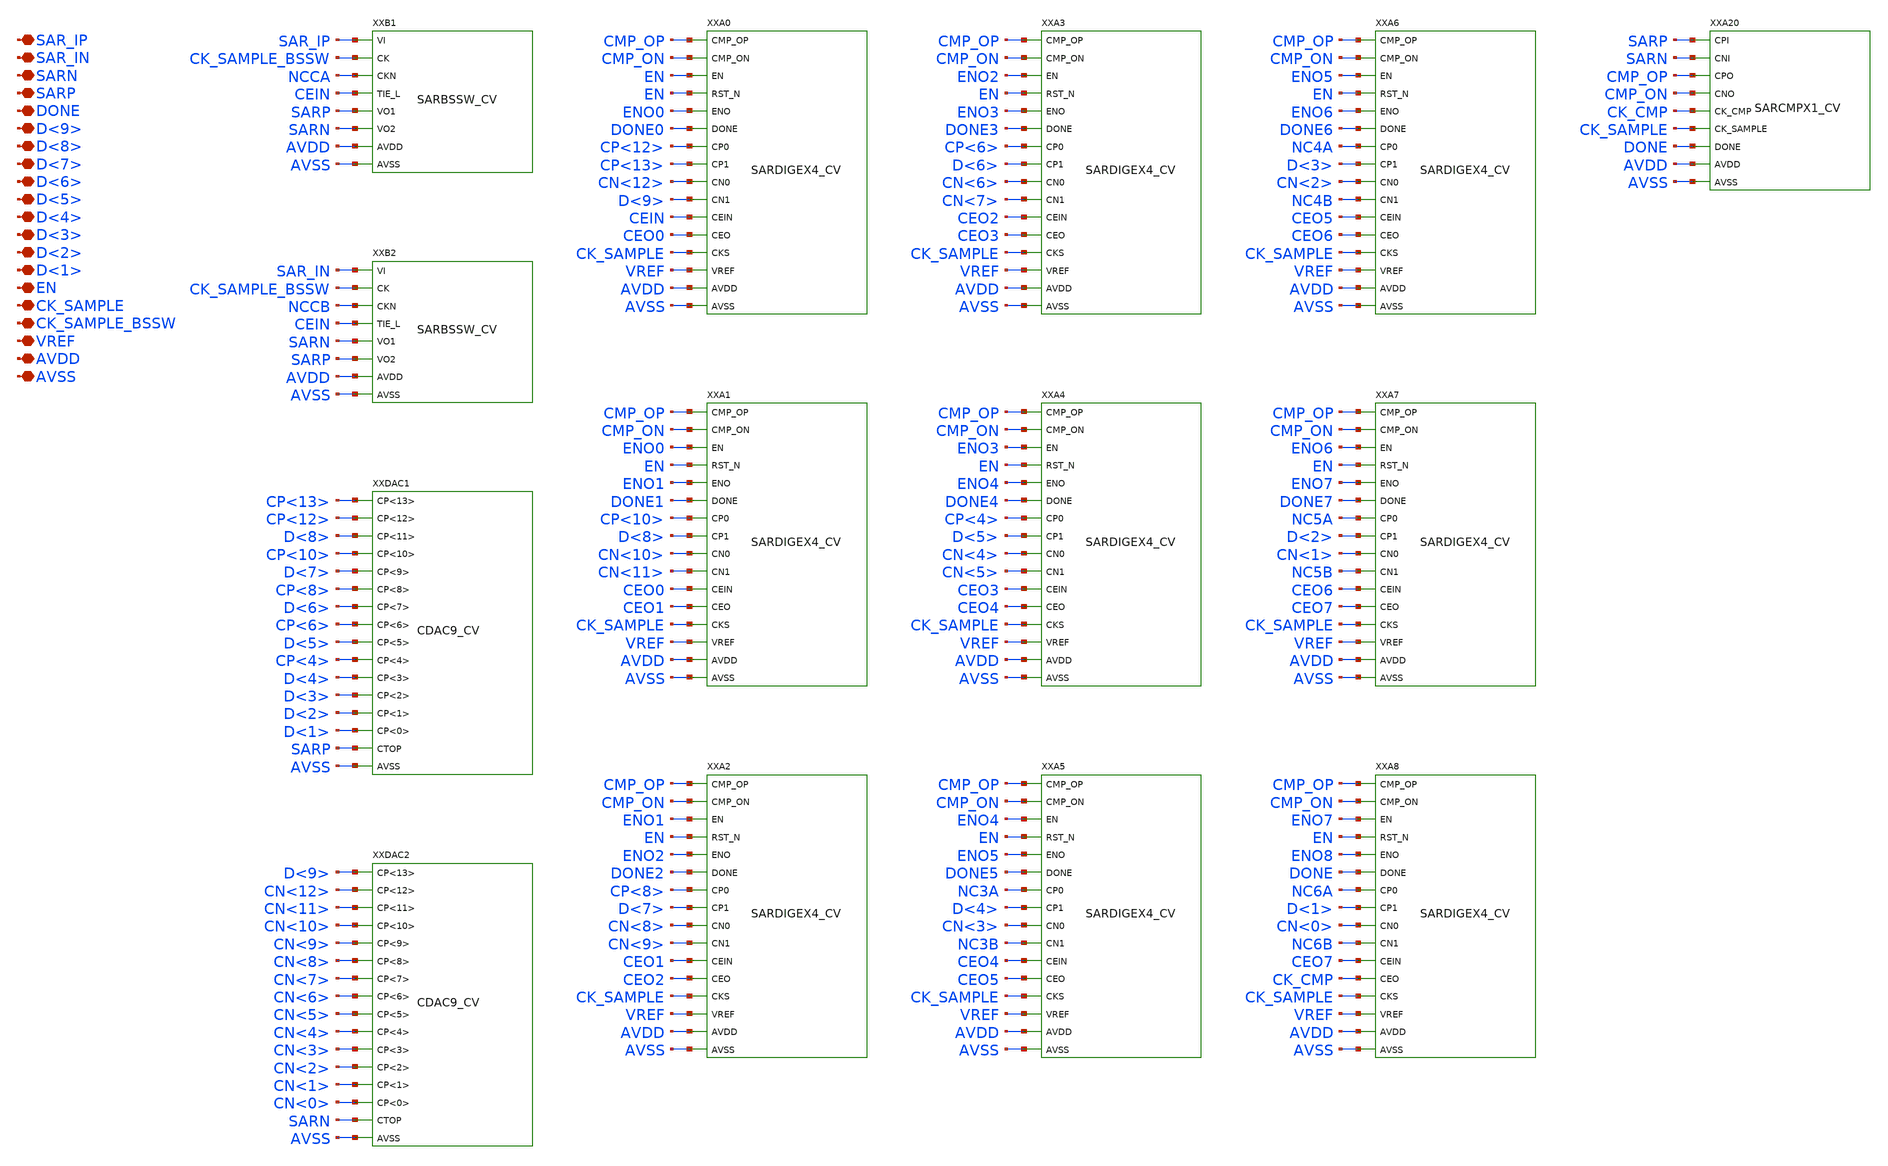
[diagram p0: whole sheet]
** sch_path: tests/transpile/SAR9B/ALGIC001_SAR9B_CV_NOROUTE.sch
**.subckt ALGIC001_SAR9B_CV_NOROUTE SAR_IP SAR_IN SARN SARP DONE D<9> D<8> D<7> D<6> D<5> D<4> D<3>
*+ D<2> D<1> EN CK_SAMPLE CK_SAMPLE_BSSW VREF AVDD AVSS
*.iopin SAR_IP
*.iopin SAR_IN
*.iopin SARN
*.iopin SARP
*.iopin DONE
*.iopin D<9>
*.iopin D<8>
*.iopin D<7>
*.iopin D<6>
*.iopin D<5>
*.iopin D<4>
*.iopin D<3>
*.iopin D<2>
*.iopin D<1>
*.iopin EN
*.iopin CK_SAMPLE
*.iopin CK_SAMPLE_BSSW
*.iopin VREF
*.iopin AVDD
*.iopin AVSS
XXB1 SAR_IP CK_SAMPLE_BSSW NCCA CEIN SARP SARN AVDD AVSS SARBSSW_CV
XXB2 SAR_IN CK_SAMPLE_BSSW NCCB CEIN SARN SARP AVDD AVSS SARBSSW_CV
XXDAC1 CP<13> CP<12> D<8> CP<10> D<7> CP<8> D<6> CP<6> D<5> CP<4> D<4> D<3> D<2> D<1> SARP AVSS
+ CDAC9_CV
XXDAC2 D<9> CN<12> CN<11> CN<10> CN<9> CN<8> CN<7> CN<6> CN<5> CN<4> CN<3> CN<2> CN<1> CN<0> SARN
+ AVSS CDAC9_CV
XXA0 CMP_OP CMP_ON EN EN ENO0 DONE0 CP<12> CP<13> CN<12> D<9> CEIN CEO0 CK_SAMPLE VREF AVDD AVSS
+ SARDIGEX4_CV
XXA1 CMP_OP CMP_ON ENO0 EN ENO1 DONE1 CP<10> D<8> CN<10> CN<11> CEO0 CEO1 CK_SAMPLE VREF AVDD AVSS
+ SARDIGEX4_CV
XXA2 CMP_OP CMP_ON ENO1 EN ENO2 DONE2 CP<8> D<7> CN<8> CN<9> CEO1 CEO2 CK_SAMPLE VREF AVDD AVSS
+ SARDIGEX4_CV
XXA3 CMP_OP CMP_ON ENO2 EN ENO3 DONE3 CP<6> D<6> CN<6> CN<7> CEO2 CEO3 CK_SAMPLE VREF AVDD AVSS
+ SARDIGEX4_CV
XXA4 CMP_OP CMP_ON ENO3 EN ENO4 DONE4 CP<4> D<5> CN<4> CN<5> CEO3 CEO4 CK_SAMPLE VREF AVDD AVSS
+ SARDIGEX4_CV
XXA5 CMP_OP CMP_ON ENO4 EN ENO5 DONE5 NC3A D<4> CN<3> NC3B CEO4 CEO5 CK_SAMPLE VREF AVDD AVSS
+ SARDIGEX4_CV
XXA6 CMP_OP CMP_ON ENO5 EN ENO6 DONE6 NC4A D<3> CN<2> NC4B CEO5 CEO6 CK_SAMPLE VREF AVDD AVSS
+ SARDIGEX4_CV
XXA7 CMP_OP CMP_ON ENO6 EN ENO7 DONE7 NC5A D<2> CN<1> NC5B CEO6 CEO7 CK_SAMPLE VREF AVDD AVSS
+ SARDIGEX4_CV
XXA8 CMP_OP CMP_ON ENO7 EN ENO8 DONE NC6A D<1> CN<0> NC6B CEO7 CK_CMP CK_SAMPLE VREF AVDD AVSS
+ SARDIGEX4_CV
XXA20 SARP SARN CMP_OP CMP_ON CK_CMP CK_SAMPLE DONE AVDD AVSS SARCMPX1_CV
**.ends
.end
